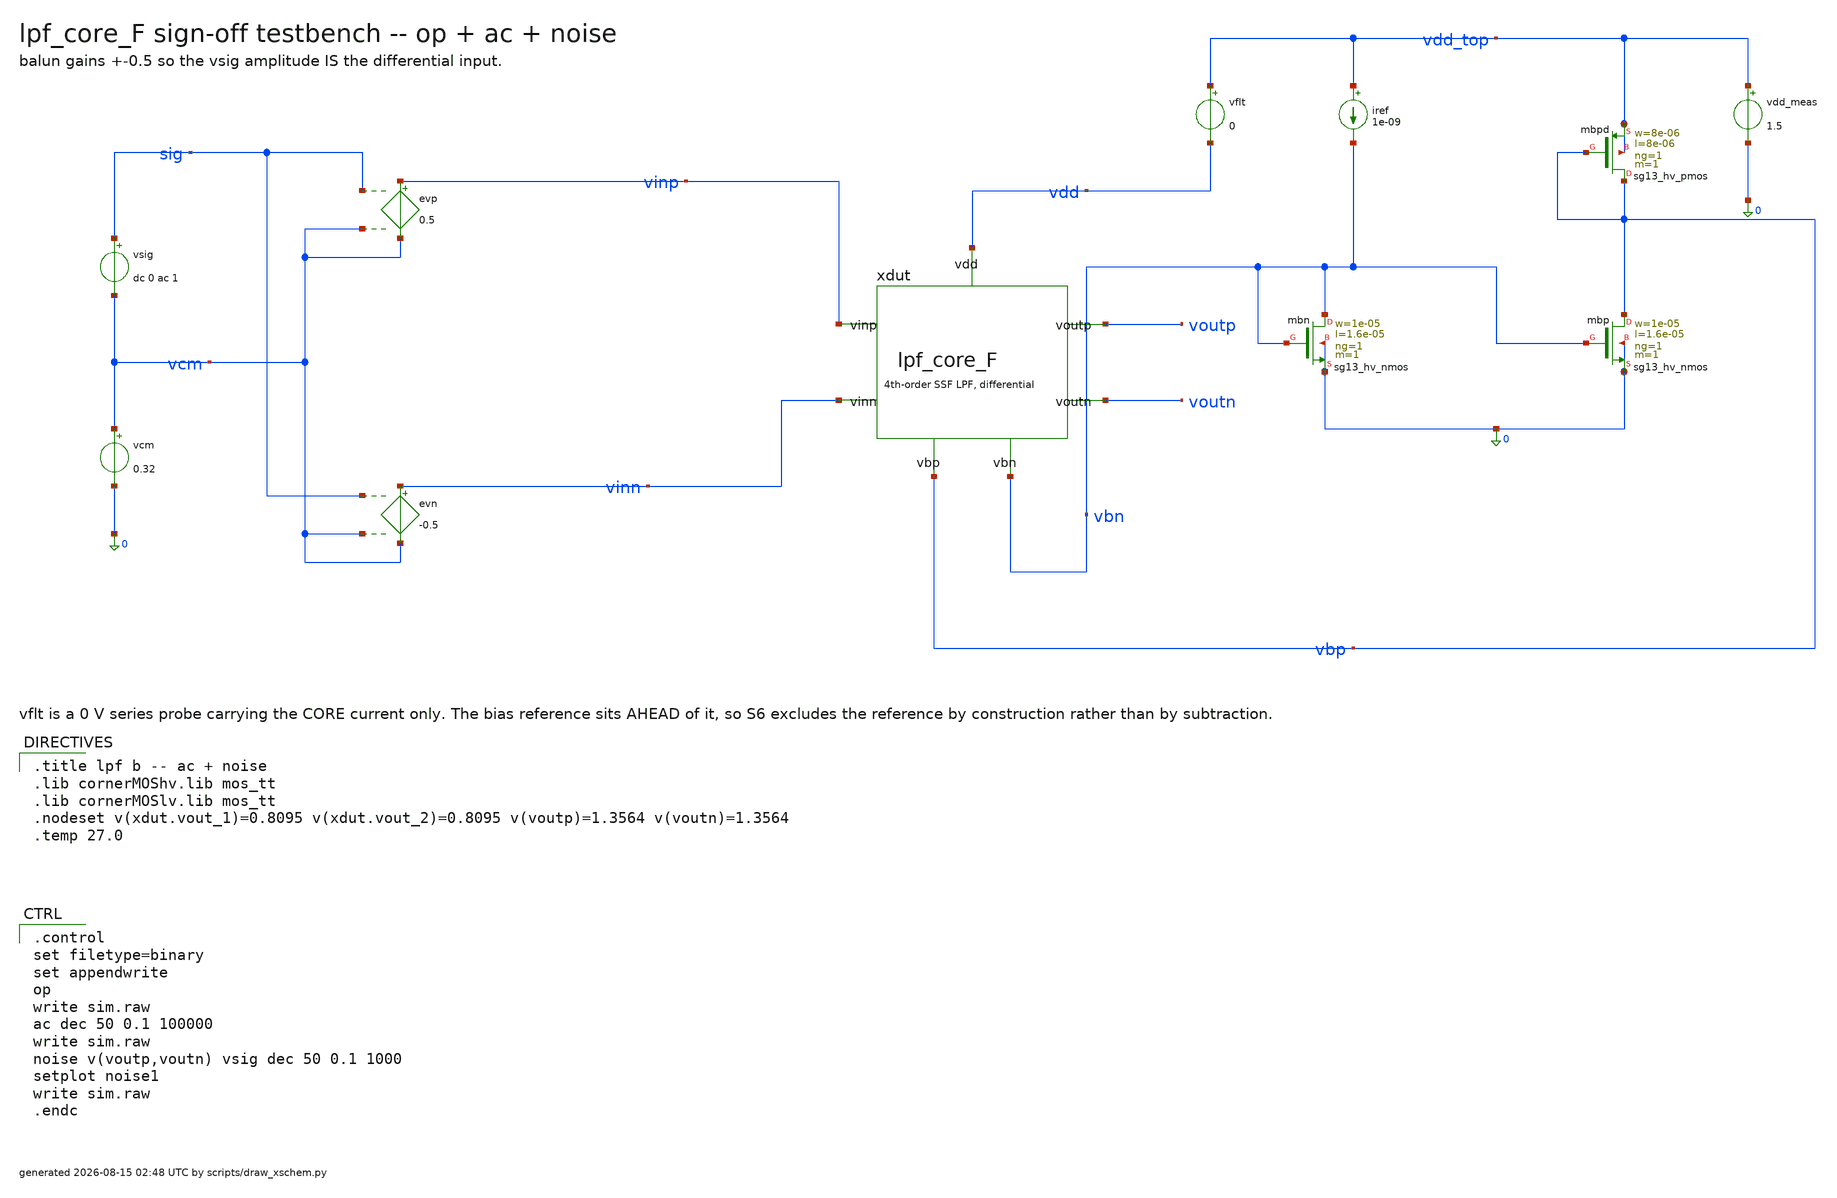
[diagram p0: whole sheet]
** sch_path: signoff/F-minnoise/lpf_tb_F.sch
**.subckt lpf_tb_F
vsig sig vcm dc 0 ac 1
vcm vcm 0 0.32
evp vinp vcm sig vcm 0.5
evn vinn vcm sig vcm -0.5
xdut vinp vinn voutp voutn vbn vbp vdd lpf_core_F
vflt vdd_top vdd 0
vdd_meas vdd_top 0 1.5
iref vdd_top vbn 1e-09
Xmbn vbn vbn 0 0 sg13_hv_nmos w=1e-05 l=1.6e-05 ng=1 m=1 mm_ok=1
Xmbp vbp vbn 0 0 sg13_hv_nmos w=1e-05 l=1.6e-05 ng=1 m=1 mm_ok=1
Xmbpd vbp vbp vdd_top vdd_top sg13_hv_pmos w=8e-06 l=8e-06 ng=1 m=1 mm_ok=1
**** begin user architecture code

.title lpf b -- ac + noise
.lib cornerMOShv.lib mos_tt
.lib cornerMOSlv.lib mos_tt
.nodeset v(xdut.vout_1)=0.8095 v(xdut.vout_2)=0.8095 v(voutp)=1.3564 v(voutn)=1.3564
.temp 27.0


.control
set filetype=binary
set appendwrite
op
write sim.raw
ac dec 50 0.1 100000
write sim.raw
noise v(voutp,voutn) vsig dec 50 0.1 1000
setplot noise1
write sim.raw
.endc

**** end user architecture code
**.ends
.end
